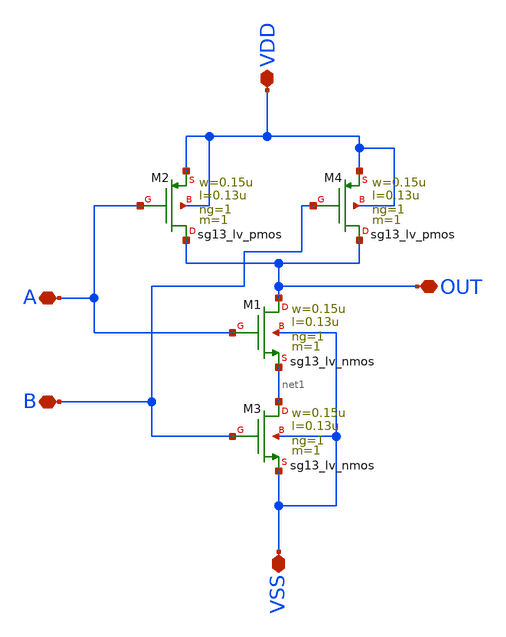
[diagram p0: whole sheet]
** sch_path: Custom_std_cells/nand_custom.sch
**.subckt nand_custom A B VDD VSS OUT
*.iopin A
*.iopin B
*.iopin VDD
*.iopin VSS
*.iopin OUT
XM1 OUT A net1 VSS sg13_lv_nmos w=0.15u l=0.13u ng=1 m=1 mm_ok=1
XM2 OUT A VDD VDD sg13_lv_pmos w=0.15u l=0.13u ng=1 m=1 mm_ok=1
XM3 net1 B VSS VSS sg13_lv_nmos w=0.15u l=0.13u ng=1 m=1 mm_ok=1
XM4 OUT B VDD VDD sg13_lv_pmos w=0.15u l=0.13u ng=1 m=1 mm_ok=1
**.ends
.end
